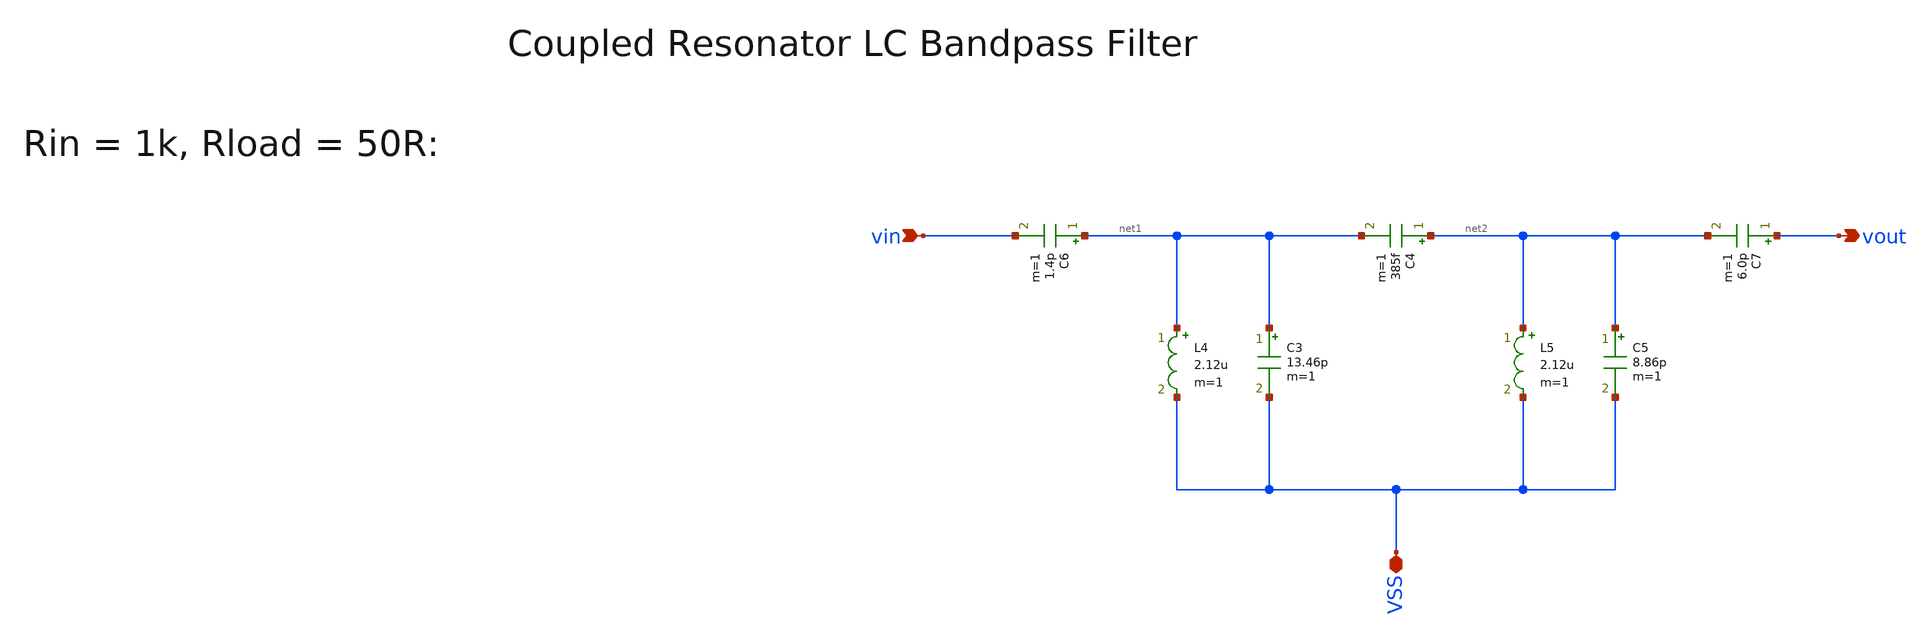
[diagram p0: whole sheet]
** sch_path: ihp130/macros/coupled_resonator_lc_bpf/schematic/xschem/coupled_resonator_lc_bpf_1k_50R.sch
**.subckt coupled_resonator_lc_bpf_1k_50R vin vout VSS
*.ipin vin
*.opin vout
*.iopin VSS
C3 net1 VSS 13.46p m=1
L4 net1 VSS 2.12u m=1
C4 net2 net1 385f m=1
C5 net2 VSS 8.86p m=1
L5 net2 VSS 2.12u m=1
C6 net1 vin 1.4p m=1
C7 vout net2 6.0p m=1
**.ends
.end
